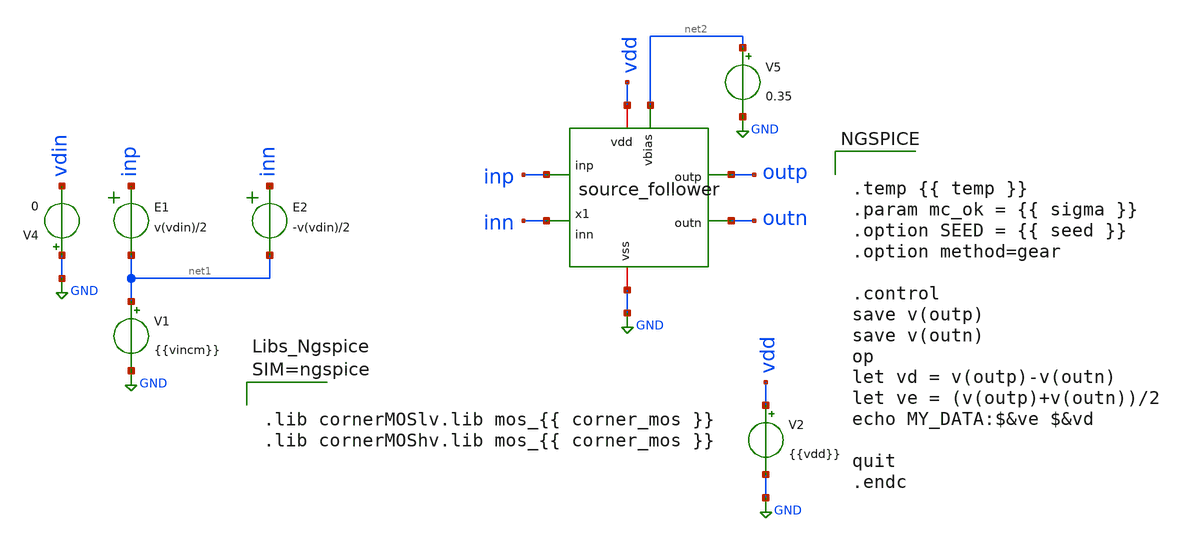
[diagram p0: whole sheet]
** sch_path: examples/source_follower/tb/tb_sf_op.sch
**.subckt tb_sf_op
E1 inp net1 VOL=' v(vdin)/2 '
E2 inn net1 VOL=' -v(vdin)/2 '
V1 net1 GND {{vincm}}
.save i(v1)
V2 vdd GND {{vdd}}
V5 net2 GND 0.35
.save i(v5)
V4 GND vdin 0
.save i(v4)
x1 vdd inn inp outp outn net2 GND source_follower
**** begin user architecture code


.temp {{ temp }}
.param mc_ok = {{ sigma }}
.option SEED = {{ seed }}
.option method=gear

.control
save v(outp)
save v(outn)
op
let vd = v(outp)-v(outn)
let ve = (v(outp)+v(outn))/2
echo MY_DATA:$&ve $&vd

quit
.endc





.lib cornerMOSlv.lib mos_{{ corner_mos }}
.lib cornerMOShv.lib mos_{{ corner_mos }}



**** end user architecture code
**.ends

* expanding   symbol:  chipify/examples/source_follower/sch/source_follower.sym # of pins=7
** sym_path: examples/source_follower/sch/source_follower.sym
** sch_path: examples/source_follower/sch/source_follower.sch
.subckt source_follower vdd inn inp outp outn vbias vss
*.ipin vbias
*.iopin vdd
*.opin outp
*.iopin vss
*.opin outn
*.ipin inp
*.ipin inn
XM1 outp vbias vss vss sg13_lv_nmos w=100u l=2u ng=20 m=1 mm_ok=1
XM2 vdd inp outp vss sg13_lv_nmos w=200u l=0.13u ng=20 m=1 mm_ok=1
XM3 outn vbias vss vss sg13_lv_nmos w=100u l=2u ng=20 m=1 mm_ok=1
XM4 vdd inn outn vss sg13_lv_nmos w=200u l=0.13u ng=20 m=1 mm_ok=1
.ends

.GLOBAL GND
.end
